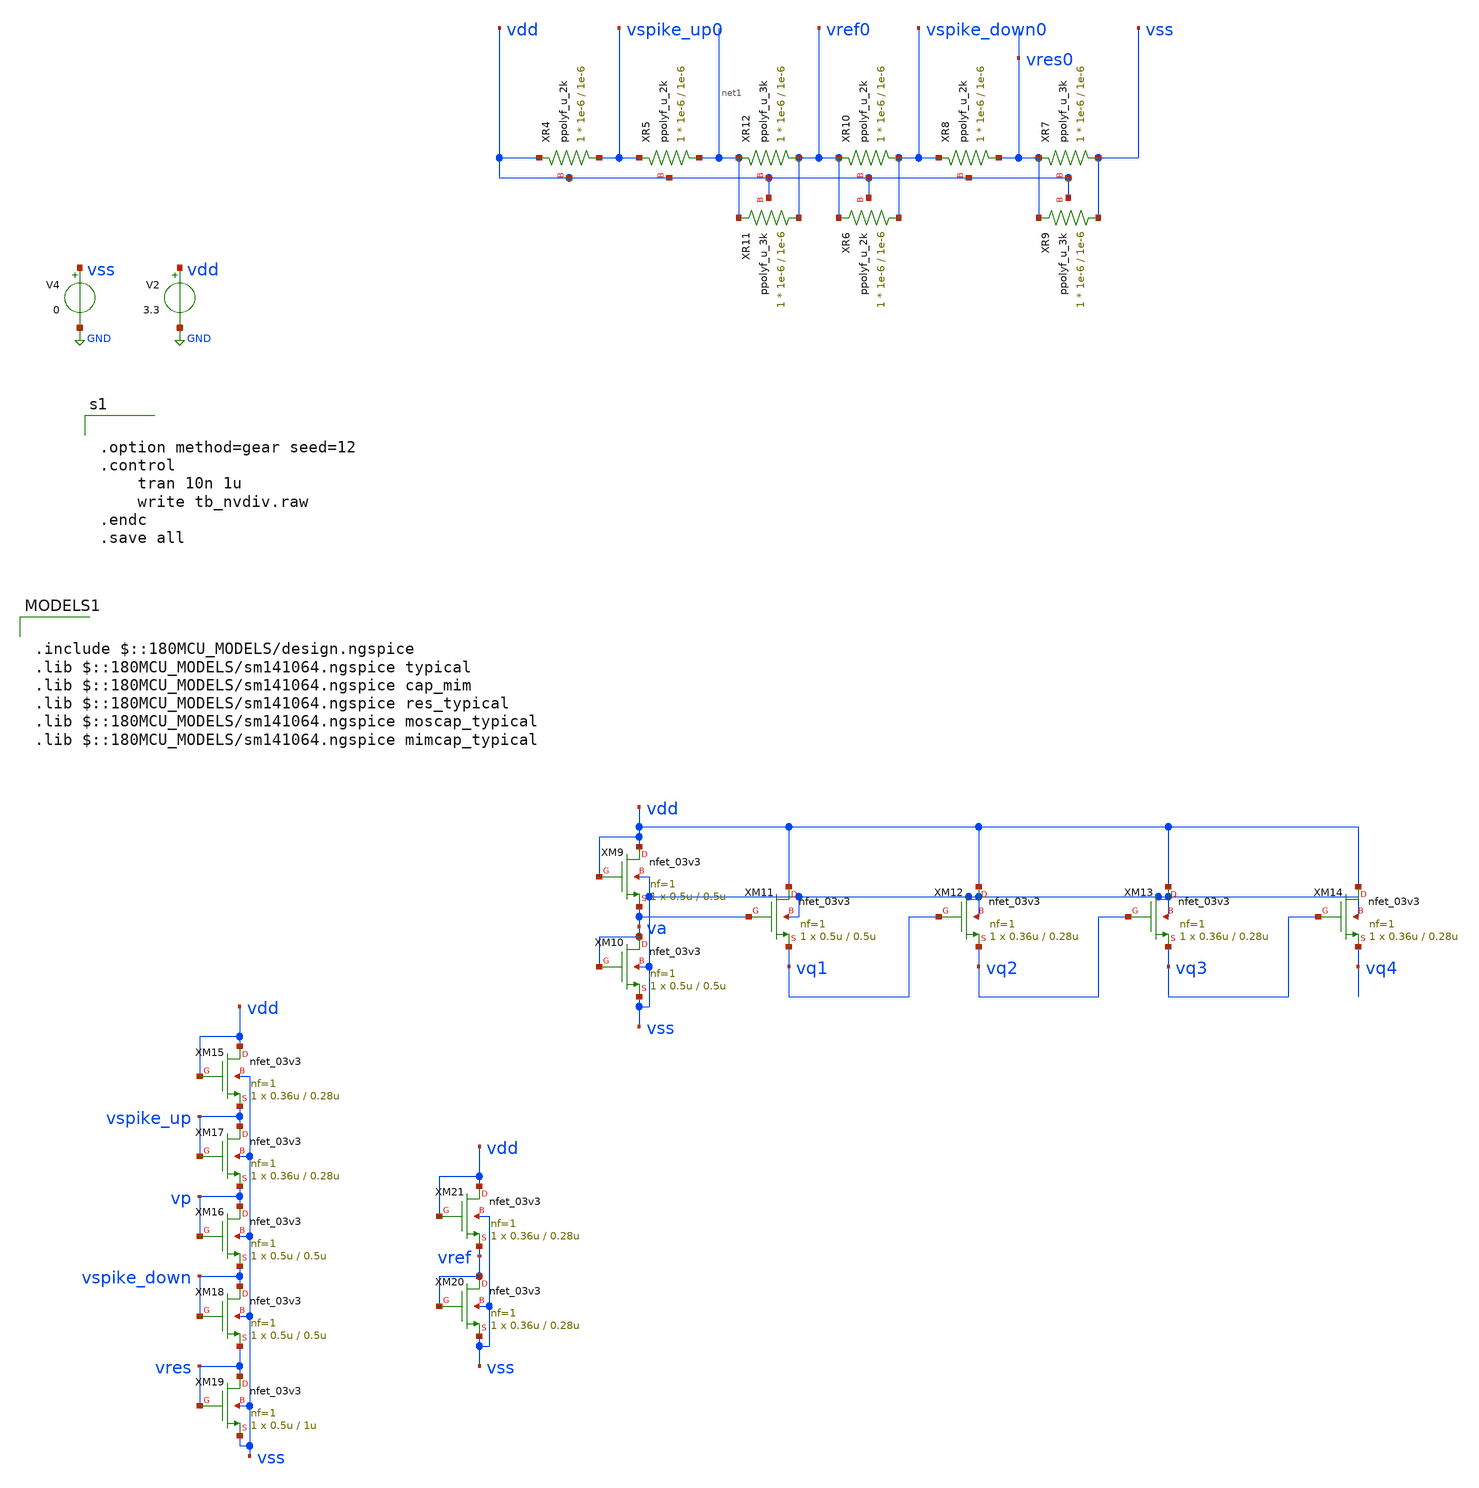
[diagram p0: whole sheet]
** sch_path: designs/libs/core_LIF_comp/tb_nvdiv.sch
**.subckt tb_nvdiv
V2 vdd GND 3.3
V4 vss GND 0
XR4 vspike_up0 vdd vdd ppolyf_u_2k r_width=1e-6 r_length=1e-6 m=1
XR5 net1 vspike_up0 vdd ppolyf_u_2k r_width=1e-6 r_length=1e-6 m=1
XR6 vspike_down0 vref0 vdd ppolyf_u_2k r_width=1e-6 r_length=1e-6 m=1
XR8 vres0 vspike_down0 vdd ppolyf_u_2k r_width=1e-6 r_length=1e-6 m=1
XR9 vss vres0 vdd ppolyf_u_3k r_width=1e-6 r_length=1e-6 m=1
XR7 vss vres0 vdd ppolyf_u_3k r_width=1e-6 r_length=1e-6 m=1
XR10 vspike_down0 vref0 vdd ppolyf_u_2k r_width=1e-6 r_length=1e-6 m=1
XR12 vref0 net1 vdd ppolyf_u_3k r_width=1e-6 r_length=1e-6 m=1
XR11 vref0 net1 vdd ppolyf_u_3k r_width=1e-6 r_length=1e-6 m=1
XM11 vdd va vq1 vss nfet_03v3 L=0.5u W=0.5u nf=1 ad='int((nf+1)/2) * W/nf * 0.18u' as='int((nf+2)/2) * W/nf * 0.18u'
+ pd='2*int((nf+1)/2) * (W/nf + 0.18u)' ps='2*int((nf+2)/2) * (W/nf + 0.18u)' nrd='0.18u / W' nrs='0.18u / W'
+ sa=0 sb=0 sd=0 m=1
XM12 vdd vq1 vq2 vss nfet_03v3 L=0.28u W=0.36u nf=1 ad='int((nf+1)/2) * W/nf * 0.18u' as='int((nf+2)/2) * W/nf * 0.18u'
+ pd='2*int((nf+1)/2) * (W/nf + 0.18u)' ps='2*int((nf+2)/2) * (W/nf + 0.18u)' nrd='0.18u / W' nrs='0.18u / W'
+ sa=0 sb=0 sd=0 m=1
XM13 vdd vq2 vq3 vss nfet_03v3 L=0.28u W=0.36u nf=1 ad='int((nf+1)/2) * W/nf * 0.18u' as='int((nf+2)/2) * W/nf * 0.18u'
+ pd='2*int((nf+1)/2) * (W/nf + 0.18u)' ps='2*int((nf+2)/2) * (W/nf + 0.18u)' nrd='0.18u / W' nrs='0.18u / W'
+ sa=0 sb=0 sd=0 m=1
XM14 vdd vq3 vq4 vss nfet_03v3 L=0.28u W=0.36u nf=1 ad='int((nf+1)/2) * W/nf * 0.18u' as='int((nf+2)/2) * W/nf * 0.18u'
+ pd='2*int((nf+1)/2) * (W/nf + 0.18u)' ps='2*int((nf+2)/2) * (W/nf + 0.18u)' nrd='0.18u / W' nrs='0.18u / W'
+ sa=0 sb=0 sd=0 m=1
XM9 vdd vdd va vss nfet_03v3 L=0.5u W=0.5u nf=1 ad='int((nf+1)/2) * W/nf * 0.18u' as='int((nf+2)/2) * W/nf * 0.18u'
+ pd='2*int((nf+1)/2) * (W/nf + 0.18u)' ps='2*int((nf+2)/2) * (W/nf + 0.18u)' nrd='0.18u / W' nrs='0.18u / W'
+ sa=0 sb=0 sd=0 m=1
XM10 va va vss vss nfet_03v3 L=0.5u W=0.5u nf=1 ad='int((nf+1)/2) * W/nf * 0.18u' as='int((nf+2)/2) * W/nf * 0.18u'
+ pd='2*int((nf+1)/2) * (W/nf + 0.18u)' ps='2*int((nf+2)/2) * (W/nf + 0.18u)' nrd='0.18u / W' nrs='0.18u / W'
+ sa=0 sb=0 sd=0 m=1
XM15 vdd vdd vspike_up vss nfet_03v3 L=0.28u W=0.36u nf=1 ad='int((nf+1)/2) * W/nf * 0.18u' as='int((nf+2)/2) * W/nf * 0.18u'
+ pd='2*int((nf+1)/2) * (W/nf + 0.18u)' ps='2*int((nf+2)/2) * (W/nf + 0.18u)' nrd='0.18u / W' nrs='0.18u / W'
+ sa=0 sb=0 sd=0 m=1
XM18 vspike_down vspike_down vres vss nfet_03v3 L=0.5u W=0.5u nf=1 ad='int((nf+1)/2) * W/nf * 0.18u'
+ as='int((nf+2)/2) * W/nf * 0.18u' pd='2*int((nf+1)/2) * (W/nf + 0.18u)' ps='2*int((nf+2)/2) * (W/nf + 0.18u)'
+ nrd='0.18u / W' nrs='0.18u / W' sa=0 sb=0 sd=0 m=1
XM16 vp vp vspike_down vss nfet_03v3 L=0.5u W=0.5u nf=1 ad='int((nf+1)/2) * W/nf * 0.18u' as='int((nf+2)/2) * W/nf * 0.18u'
+ pd='2*int((nf+1)/2) * (W/nf + 0.18u)' ps='2*int((nf+2)/2) * (W/nf + 0.18u)' nrd='0.18u / W' nrs='0.18u / W'
+ sa=0 sb=0 sd=0 m=1
XM19 vres vres vss vss nfet_03v3 L=1u W=0.5u nf=1 ad='int((nf+1)/2) * W/nf * 0.18u' as='int((nf+2)/2) * W/nf * 0.18u'
+ pd='2*int((nf+1)/2) * (W/nf + 0.18u)' ps='2*int((nf+2)/2) * (W/nf + 0.18u)' nrd='0.18u / W' nrs='0.18u / W'
+ sa=0 sb=0 sd=0 m=1
XM17 vspike_up vspike_up vp vss nfet_03v3 L=0.28u W=0.36u nf=1 ad='int((nf+1)/2) * W/nf * 0.18u' as='int((nf+2)/2) * W/nf * 0.18u'
+ pd='2*int((nf+1)/2) * (W/nf + 0.18u)' ps='2*int((nf+2)/2) * (W/nf + 0.18u)' nrd='0.18u / W' nrs='0.18u / W'
+ sa=0 sb=0 sd=0 m=1
XM20 vref vref vss vss nfet_03v3 L=0.28u W=0.36u nf=1 ad='int((nf+1)/2) * W/nf * 0.18u' as='int((nf+2)/2) * W/nf * 0.18u'
+ pd='2*int((nf+1)/2) * (W/nf + 0.18u)' ps='2*int((nf+2)/2) * (W/nf + 0.18u)' nrd='0.18u / W' nrs='0.18u / W'
+ sa=0 sb=0 sd=0 m=1
XM21 vdd vdd vref vss nfet_03v3 L=0.28u W=0.36u nf=1 ad='int((nf+1)/2) * W/nf * 0.18u' as='int((nf+2)/2) * W/nf * 0.18u'
+ pd='2*int((nf+1)/2) * (W/nf + 0.18u)' ps='2*int((nf+2)/2) * (W/nf + 0.18u)' nrd='0.18u / W' nrs='0.18u / W'
+ sa=0 sb=0 sd=0 m=1
**** begin user architecture code


.option method=gear seed=12
.control
    tran 10n 1u
    write tb_nvdiv.raw
.endc
.save all



.include $::180MCU_MODELS/design.ngspice
.lib $::180MCU_MODELS/sm141064.ngspice typical
.lib $::180MCU_MODELS/sm141064.ngspice cap_mim
.lib $::180MCU_MODELS/sm141064.ngspice res_typical
.lib $::180MCU_MODELS/sm141064.ngspice moscap_typical
.lib $::180MCU_MODELS/sm141064.ngspice mimcap_typical

**** end user architecture code
**.ends
.GLOBAL GND
.end
